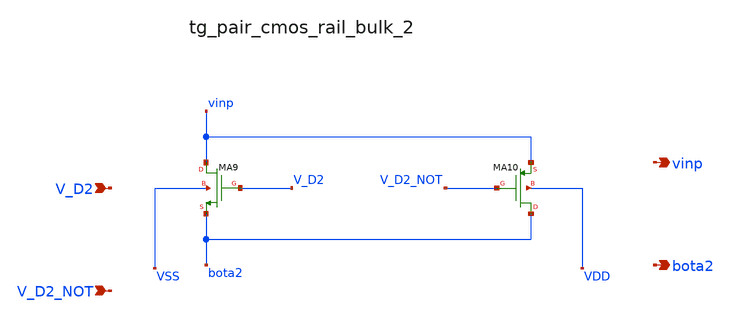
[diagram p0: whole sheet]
** sch_path: analog-db/raw/ia_005_hsu_pga_ideal/hier/blocks/tg_pair_cmos_rail_bulk_2.sch
**.subckt tg_pair_cmos_rail_bulk_2 V_D2 V_D2_NOT vinp bota2
*.ipin V_D2
*.ipin V_D2_NOT
*.opin vinp
*.opin bota2
XMA10 bota2 V_D2_NOT vinp VDD sg13_lv_pmos w=x_dut_xma10_w l=x_dut_xma10_l ng=1 m=x_dut_xma10_m
XMA9 vinp V_D2 bota2 VSS sg13_lv_nmos w=x_dut_xma9_w l=x_dut_xma9_l ng=1 m=x_dut_xma9_m
**.ends
.end
